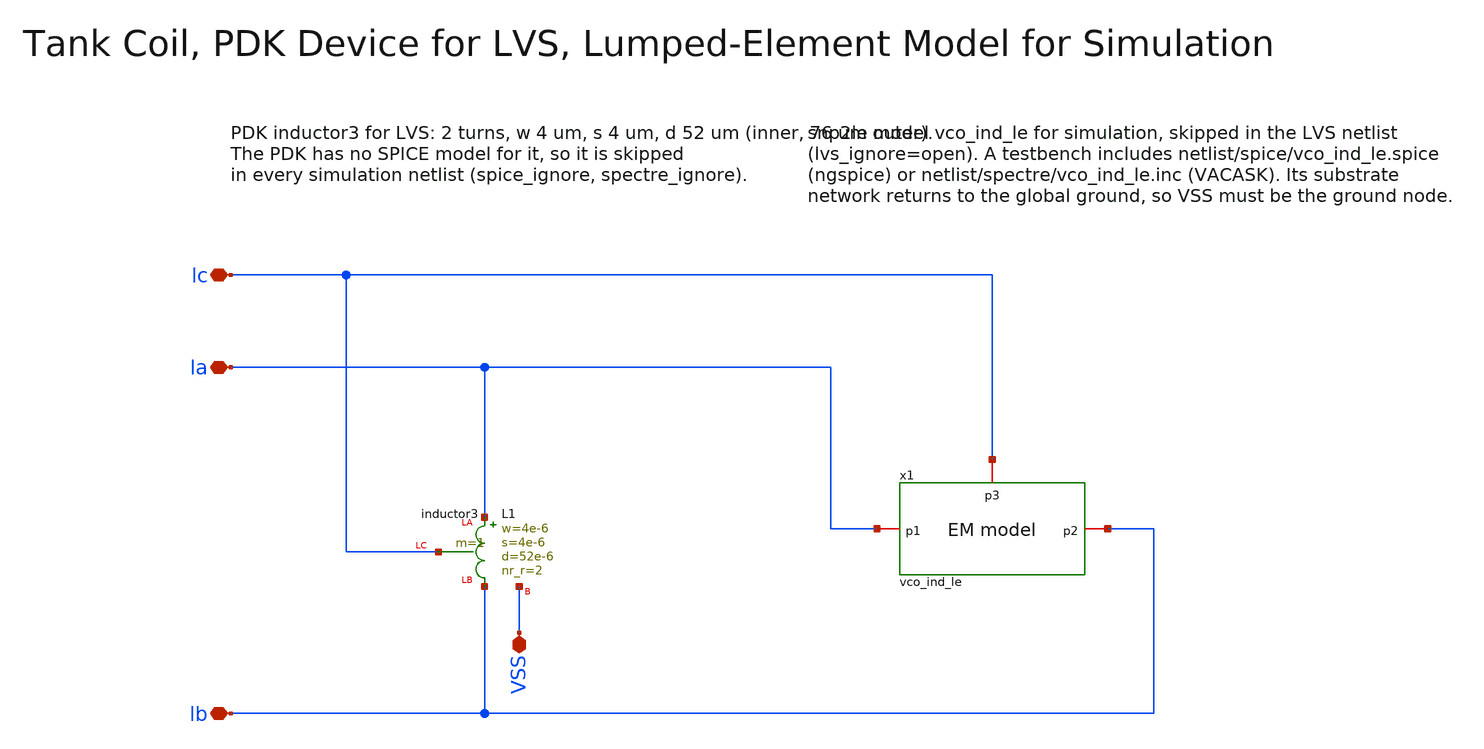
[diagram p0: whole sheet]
** sch_path: macros/vco/schematic/xschem/vco_ind.sch
**.subckt vco_ind la lc lb VSS
*.iopin la
*.iopin lc
*.iopin lb
*.iopin VSS
XL1 la lc lb VSS inductor3 w=4e-6 s=4e-6 d=52e-6 nr_r=2 m=1
x1 la lb lc vco_ind_le
**.ends
.end
